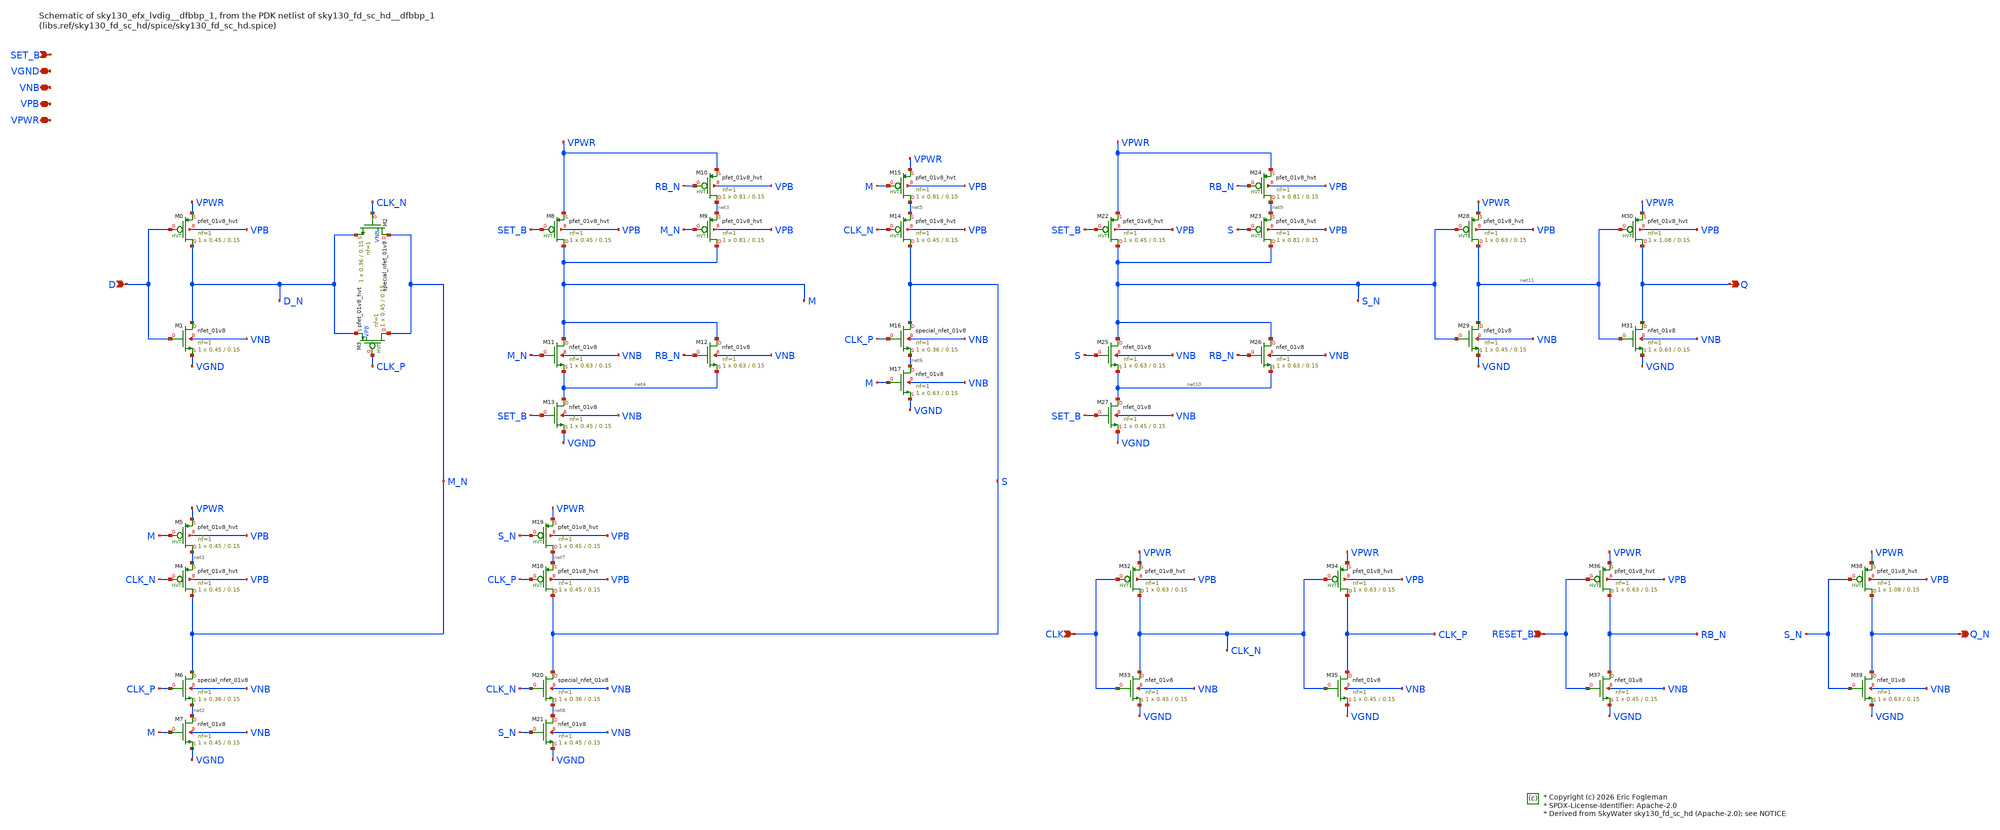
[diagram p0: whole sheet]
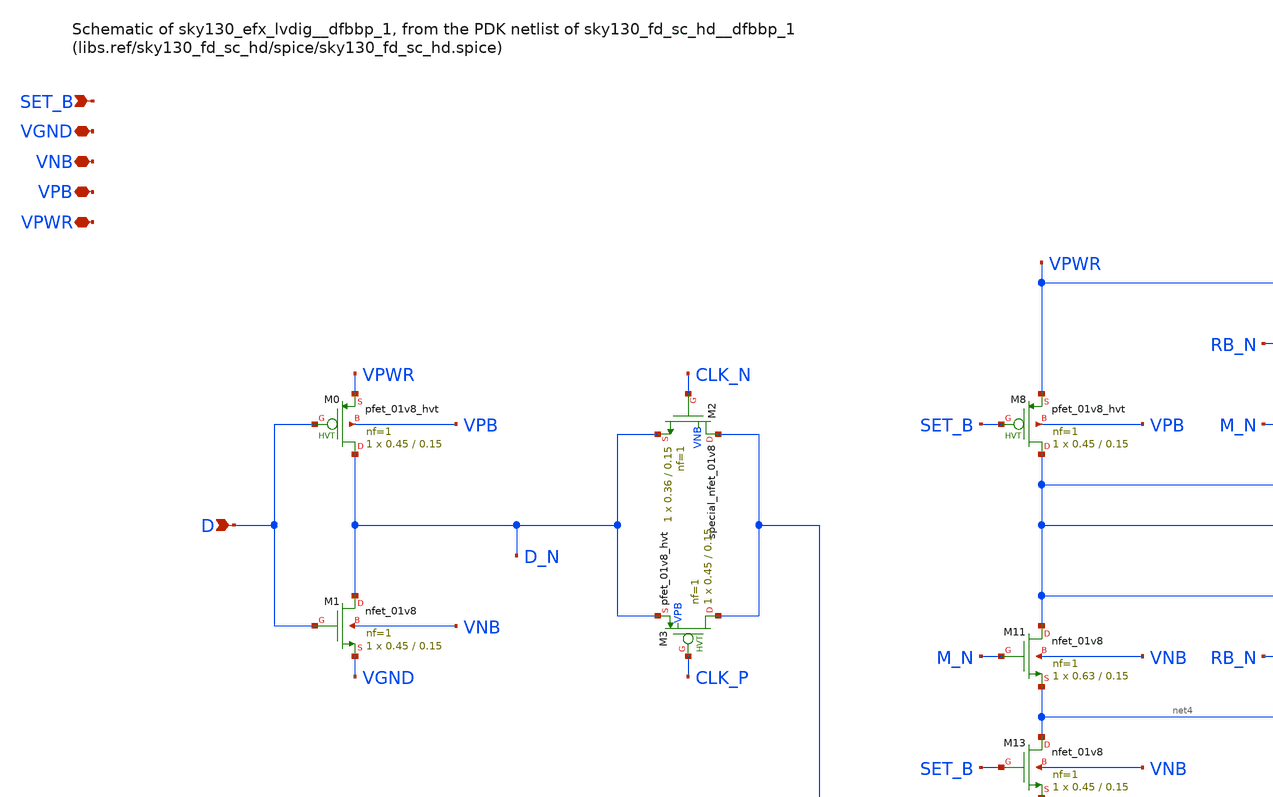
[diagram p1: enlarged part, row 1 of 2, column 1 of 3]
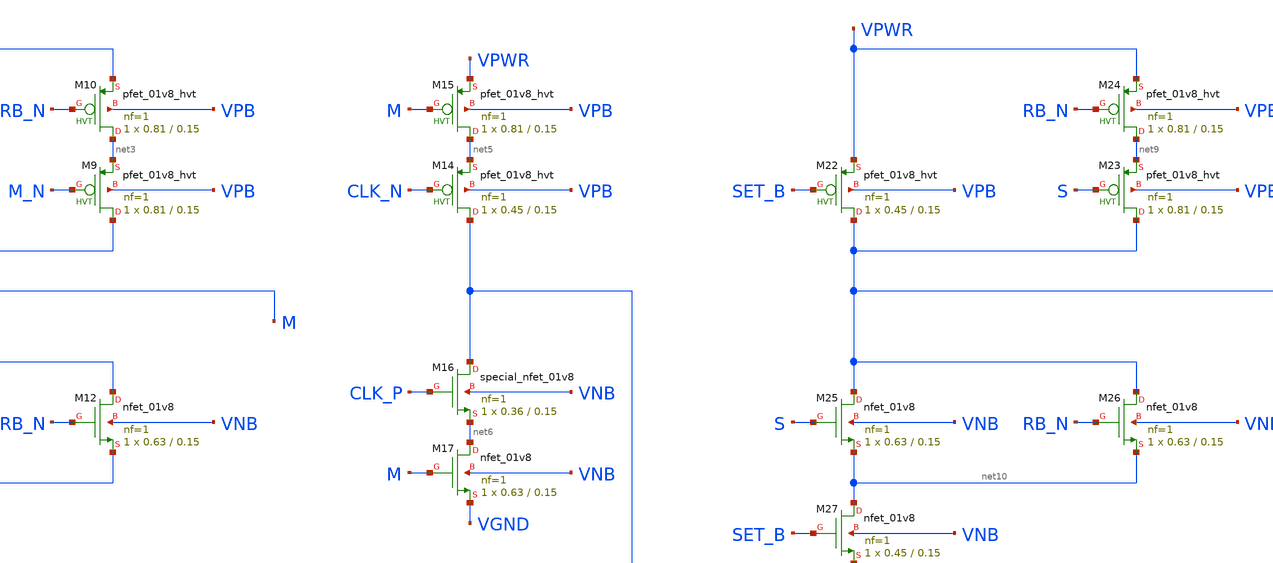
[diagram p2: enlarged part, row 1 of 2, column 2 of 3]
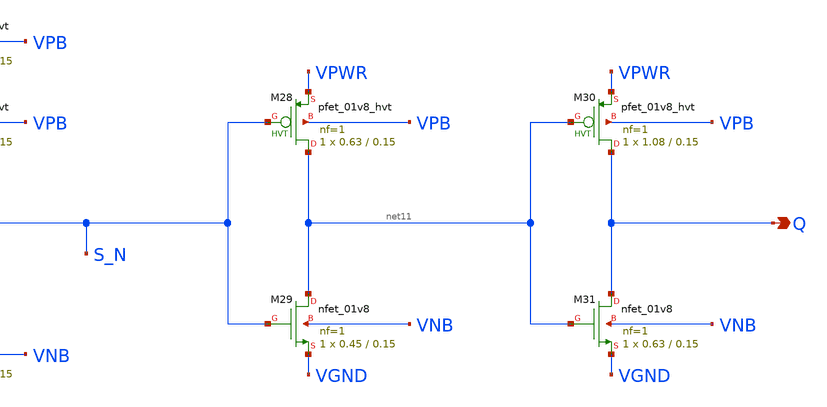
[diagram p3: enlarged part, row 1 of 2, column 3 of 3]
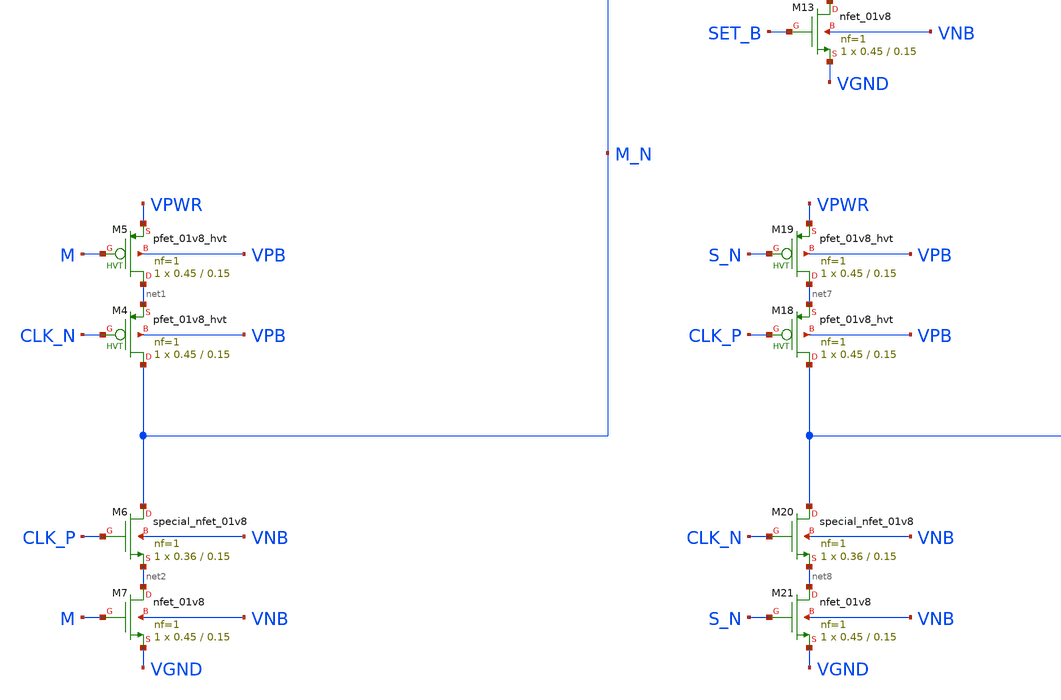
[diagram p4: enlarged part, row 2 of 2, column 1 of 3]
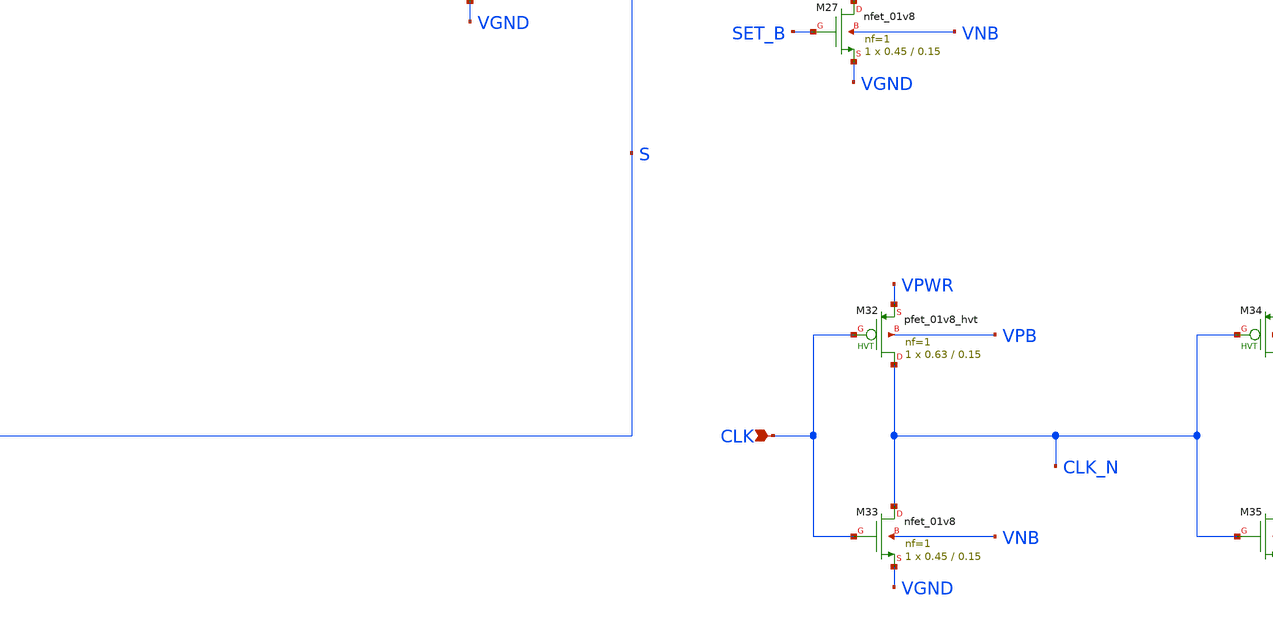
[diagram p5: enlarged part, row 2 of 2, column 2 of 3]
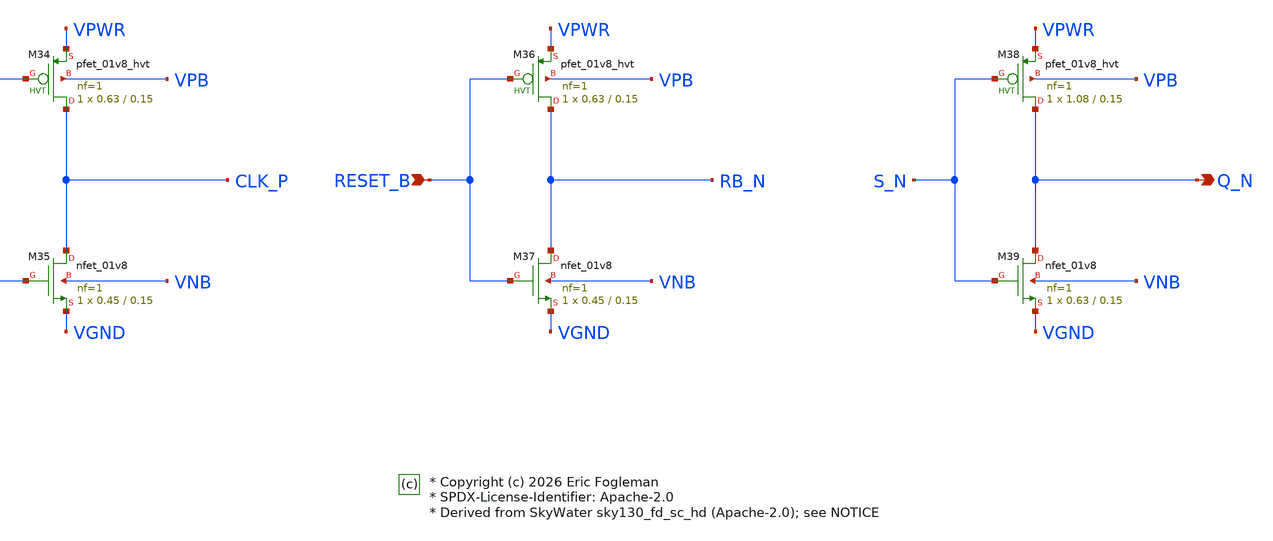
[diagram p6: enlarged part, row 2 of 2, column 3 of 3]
** sch_path: xschem/sky130_efx_lvdig__dfbbp_1.sch

* Copyright (c) 2026 Eric Fogleman
* SPDX-License-Identifier: Apache-2.0
* Derived from SkyWater sky130_fd_sc_hd (Apache-2.0); see NOTICE

**.subckt sky130_efx_lvdig__dfbbp_1 D Q CLK RESET_B Q_N SET_B VGND VNB VPB VPWR
*.ipin D
*.opin Q
*.ipin CLK
*.ipin RESET_B
*.opin Q_N
*.ipin SET_B
*.iopin VGND
*.iopin VNB
*.iopin VPB
*.iopin VPWR
XM0 D_N D VPWR VPB sky130_fd_pr__pfet_01v8_hvt L=0.15 W=0.45 nf=1 ad='int((1 + 1)/2) * 0.45 / 1 * 0.29'
+ as='int((1 + 2)/2) * 0.45 / 1 * 0.29' pd='2*int((1 + 1)/2) * (0.45 / 1 + 0.29)' ps='2*int((1 + 2)/2) * (0.45 / 1 + 0.29)'
+ nrd='0.29 / 0.45 ' nrs='0.29 / 0.45 ' sa=0 sb=0 sd=0 mult=1 m=1
XM1 D_N D VGND VNB sky130_fd_pr__nfet_01v8 L=0.15 W=0.45 nf=1 ad='int((1 + 1)/2) * 0.45 / 1 * 0.29' as='int((1 + 2)/2) * 0.45 / 1 * 0.29'
+ pd='2*int((1 + 1)/2) * (0.45 / 1 + 0.29)' ps='2*int((1 + 2)/2) * (0.45 / 1 + 0.29)' nrd='0.29 / 0.45 '
+ nrs='0.29 / 0.45 ' sa=0 sb=0 sd=0 mult=1 m=1
XM2 M_N CLK_N D_N VNB sky130_fd_pr__special_nfet_01v8 L=0.15 W=0.36 nf=1 ad='int((nf+1)/2) * W/nf * 0.29'
+ as='int((nf+2)/2) * W/nf * 0.29' pd='2*int((nf+1)/2) * (W/nf + 0.29)' ps='2*int((nf+2)/2) * (W/nf + 0.29)'
+ nrd='0.29 / W' nrs='0.29 / W' sa=0 sb=0 sd=0 mult=1 m=1
XM3 M_N CLK_P D_N VPB sky130_fd_pr__pfet_01v8_hvt L=0.15 W=0.45 nf=1 ad='int((1 + 1)/2) * 0.45 / 1 * 0.29'
+ as='int((1 + 2)/2) * 0.45 / 1 * 0.29' pd='2*int((1 + 1)/2) * (0.45 / 1 + 0.29)' ps='2*int((1 + 2)/2) * (0.45 / 1 + 0.29)'
+ nrd='0.29 / 0.45 ' nrs='0.29 / 0.45 ' sa=0 sb=0 sd=0 mult=1 m=1
XM4 M_N CLK_N net1 VPB sky130_fd_pr__pfet_01v8_hvt L=0.15 W=0.45 nf=1 ad='int((1 + 1)/2) * 0.45 / 1 * 0.29'
+ as='int((1 + 2)/2) * 0.45 / 1 * 0.29' pd='2*int((1 + 1)/2) * (0.45 / 1 + 0.29)' ps='2*int((1 + 2)/2) * (0.45 / 1 + 0.29)'
+ nrd='0.29 / 0.45 ' nrs='0.29 / 0.45 ' sa=0 sb=0 sd=0 mult=1 m=1
XM5 net1 M VPWR VPB sky130_fd_pr__pfet_01v8_hvt L=0.15 W=0.45 nf=1 ad='int((1 + 1)/2) * 0.45 / 1 * 0.29'
+ as='int((1 + 2)/2) * 0.45 / 1 * 0.29' pd='2*int((1 + 1)/2) * (0.45 / 1 + 0.29)' ps='2*int((1 + 2)/2) * (0.45 / 1 + 0.29)'
+ nrd='0.29 / 0.45 ' nrs='0.29 / 0.45 ' sa=0 sb=0 sd=0 mult=1 m=1
XM6 M_N CLK_P net2 VNB sky130_fd_pr__special_nfet_01v8 L=0.15 W=0.36 nf=1 ad='int((1 + 1)/2) * 0.36 / 1 * 0.29'
+ as='int((1 + 2)/2) * 0.36 / 1 * 0.29' pd='2*int((1 + 1)/2) * (0.36 / 1 + 0.29)' ps='2*int((1 + 2)/2) * (0.36 / 1 + 0.29)'
+ nrd='0.29 / 0.36 ' nrs='0.29 / 0.36 ' sa=0 sb=0 sd=0 mult=1 m=1
XM7 net2 M VGND VNB sky130_fd_pr__nfet_01v8 L=0.15 W=0.45 nf=1 ad='int((1 + 1)/2) * 0.45 / 1 * 0.29'
+ as='int((1 + 2)/2) * 0.45 / 1 * 0.29' pd='2*int((1 + 1)/2) * (0.45 / 1 + 0.29)' ps='2*int((1 + 2)/2) * (0.45 / 1 + 0.29)'
+ nrd='0.29 / 0.45 ' nrs='0.29 / 0.45 ' sa=0 sb=0 sd=0 mult=1 m=1
XM8 M SET_B VPWR VPB sky130_fd_pr__pfet_01v8_hvt L=0.15 W=0.45 nf=1 ad='int((1 + 1)/2) * 0.45 / 1 * 0.29'
+ as='int((1 + 2)/2) * 0.45 / 1 * 0.29' pd='2*int((1 + 1)/2) * (0.45 / 1 + 0.29)' ps='2*int((1 + 2)/2) * (0.45 / 1 + 0.29)'
+ nrd='0.29 / 0.45 ' nrs='0.29 / 0.45 ' sa=0 sb=0 sd=0 mult=1 m=1
XM9 M M_N net3 VPB sky130_fd_pr__pfet_01v8_hvt L=0.15 W=0.81 nf=1 ad='int((1 + 1)/2) * 0.81 / 1 * 0.29'
+ as='int((1 + 2)/2) * 0.81 / 1 * 0.29' pd='2*int((1 + 1)/2) * (0.81 / 1 + 0.29)' ps='2*int((1 + 2)/2) * (0.81 / 1 + 0.29)'
+ nrd='0.29 / 0.81 ' nrs='0.29 / 0.81 ' sa=0 sb=0 sd=0 mult=1 m=1
XM10 net3 RB_N VPWR VPB sky130_fd_pr__pfet_01v8_hvt L=0.15 W=0.81 nf=1 ad='int((1 + 1)/2) * 0.81 / 1 * 0.29'
+ as='int((1 + 2)/2) * 0.81 / 1 * 0.29' pd='2*int((1 + 1)/2) * (0.81 / 1 + 0.29)' ps='2*int((1 + 2)/2) * (0.81 / 1 + 0.29)'
+ nrd='0.29 / 0.81 ' nrs='0.29 / 0.81 ' sa=0 sb=0 sd=0 mult=1 m=1
XM11 M M_N net4 VNB sky130_fd_pr__nfet_01v8 L=0.15 W=0.63 nf=1 ad='int((1 + 1)/2) * 0.63 / 1 * 0.29'
+ as='int((1 + 2)/2) * 0.63 / 1 * 0.29' pd='2*int((1 + 1)/2) * (0.63 / 1 + 0.29)' ps='2*int((1 + 2)/2) * (0.63 / 1 + 0.29)'
+ nrd='0.29 / 0.63 ' nrs='0.29 / 0.63 ' sa=0 sb=0 sd=0 mult=1 m=1
XM12 M RB_N net4 VNB sky130_fd_pr__nfet_01v8 L=0.15 W=0.63 nf=1 ad='int((1 + 1)/2) * 0.63 / 1 * 0.29'
+ as='int((1 + 2)/2) * 0.63 / 1 * 0.29' pd='2*int((1 + 1)/2) * (0.63 / 1 + 0.29)' ps='2*int((1 + 2)/2) * (0.63 / 1 + 0.29)'
+ nrd='0.29 / 0.63 ' nrs='0.29 / 0.63 ' sa=0 sb=0 sd=0 mult=1 m=1
XM13 net4 SET_B VGND VNB sky130_fd_pr__nfet_01v8 L=0.15 W=0.45 nf=1 ad='int((1 + 1)/2) * 0.45 / 1 * 0.29'
+ as='int((1 + 2)/2) * 0.45 / 1 * 0.29' pd='2*int((1 + 1)/2) * (0.45 / 1 + 0.29)' ps='2*int((1 + 2)/2) * (0.45 / 1 + 0.29)'
+ nrd='0.29 / 0.45 ' nrs='0.29 / 0.45 ' sa=0 sb=0 sd=0 mult=1 m=1
XM14 S CLK_N net5 VPB sky130_fd_pr__pfet_01v8_hvt L=0.15 W=0.45 nf=1 ad='int((1 + 1)/2) * 0.45 / 1 * 0.29'
+ as='int((1 + 2)/2) * 0.45 / 1 * 0.29' pd='2*int((1 + 1)/2) * (0.45 / 1 + 0.29)' ps='2*int((1 + 2)/2) * (0.45 / 1 + 0.29)'
+ nrd='0.29 / 0.45 ' nrs='0.29 / 0.45 ' sa=0 sb=0 sd=0 mult=1 m=1
XM15 net5 M VPWR VPB sky130_fd_pr__pfet_01v8_hvt L=0.15 W=0.81 nf=1 ad='int((1 + 1)/2) * 0.81 / 1 * 0.29'
+ as='int((1 + 2)/2) * 0.81 / 1 * 0.29' pd='2*int((1 + 1)/2) * (0.81 / 1 + 0.29)' ps='2*int((1 + 2)/2) * (0.81 / 1 + 0.29)'
+ nrd='0.29 / 0.81 ' nrs='0.29 / 0.81 ' sa=0 sb=0 sd=0 mult=1 m=1
XM16 S CLK_P net6 VNB sky130_fd_pr__special_nfet_01v8 L=0.15 W=0.36 nf=1 ad='int((1 + 1)/2) * 0.36 / 1 * 0.29'
+ as='int((1 + 2)/2) * 0.36 / 1 * 0.29' pd='2*int((1 + 1)/2) * (0.36 / 1 + 0.29)' ps='2*int((1 + 2)/2) * (0.36 / 1 + 0.29)'
+ nrd='0.29 / 0.36 ' nrs='0.29 / 0.36 ' sa=0 sb=0 sd=0 mult=1 m=1
XM17 net6 M VGND VNB sky130_fd_pr__nfet_01v8 L=0.15 W=0.63 nf=1 ad='int((1 + 1)/2) * 0.63 / 1 * 0.29'
+ as='int((1 + 2)/2) * 0.63 / 1 * 0.29' pd='2*int((1 + 1)/2) * (0.63 / 1 + 0.29)' ps='2*int((1 + 2)/2) * (0.63 / 1 + 0.29)'
+ nrd='0.29 / 0.63 ' nrs='0.29 / 0.63 ' sa=0 sb=0 sd=0 mult=1 m=1
XM18 S CLK_P net7 VPB sky130_fd_pr__pfet_01v8_hvt L=0.15 W=0.45 nf=1 ad='int((1 + 1)/2) * 0.45 / 1 * 0.29'
+ as='int((1 + 2)/2) * 0.45 / 1 * 0.29' pd='2*int((1 + 1)/2) * (0.45 / 1 + 0.29)' ps='2*int((1 + 2)/2) * (0.45 / 1 + 0.29)'
+ nrd='0.29 / 0.45 ' nrs='0.29 / 0.45 ' sa=0 sb=0 sd=0 mult=1 m=1
XM19 net7 S_N VPWR VPB sky130_fd_pr__pfet_01v8_hvt L=0.15 W=0.45 nf=1 ad='int((1 + 1)/2) * 0.45 / 1 * 0.29'
+ as='int((1 + 2)/2) * 0.45 / 1 * 0.29' pd='2*int((1 + 1)/2) * (0.45 / 1 + 0.29)' ps='2*int((1 + 2)/2) * (0.45 / 1 + 0.29)'
+ nrd='0.29 / 0.45 ' nrs='0.29 / 0.45 ' sa=0 sb=0 sd=0 mult=1 m=1
XM20 S CLK_N net8 VNB sky130_fd_pr__special_nfet_01v8 L=0.15 W=0.36 nf=1 ad='int((1 + 1)/2) * 0.36 / 1 * 0.29'
+ as='int((1 + 2)/2) * 0.36 / 1 * 0.29' pd='2*int((1 + 1)/2) * (0.36 / 1 + 0.29)' ps='2*int((1 + 2)/2) * (0.36 / 1 + 0.29)'
+ nrd='0.29 / 0.36 ' nrs='0.29 / 0.36 ' sa=0 sb=0 sd=0 mult=1 m=1
XM21 net8 S_N VGND VNB sky130_fd_pr__nfet_01v8 L=0.15 W=0.45 nf=1 ad='int((1 + 1)/2) * 0.45 / 1 * 0.29'
+ as='int((1 + 2)/2) * 0.45 / 1 * 0.29' pd='2*int((1 + 1)/2) * (0.45 / 1 + 0.29)' ps='2*int((1 + 2)/2) * (0.45 / 1 + 0.29)'
+ nrd='0.29 / 0.45 ' nrs='0.29 / 0.45 ' sa=0 sb=0 sd=0 mult=1 m=1
XM22 S_N SET_B VPWR VPB sky130_fd_pr__pfet_01v8_hvt L=0.15 W=0.45 nf=1 ad='int((1 + 1)/2) * 0.45 / 1 * 0.29'
+ as='int((1 + 2)/2) * 0.45 / 1 * 0.29' pd='2*int((1 + 1)/2) * (0.45 / 1 + 0.29)' ps='2*int((1 + 2)/2) * (0.45 / 1 + 0.29)'
+ nrd='0.29 / 0.45 ' nrs='0.29 / 0.45 ' sa=0 sb=0 sd=0 mult=1 m=1
XM23 S_N S net9 VPB sky130_fd_pr__pfet_01v8_hvt L=0.15 W=0.81 nf=1 ad='int((1 + 1)/2) * 0.81 / 1 * 0.29'
+ as='int((1 + 2)/2) * 0.81 / 1 * 0.29' pd='2*int((1 + 1)/2) * (0.81 / 1 + 0.29)' ps='2*int((1 + 2)/2) * (0.81 / 1 + 0.29)'
+ nrd='0.29 / 0.81 ' nrs='0.29 / 0.81 ' sa=0 sb=0 sd=0 mult=1 m=1
XM24 net9 RB_N VPWR VPB sky130_fd_pr__pfet_01v8_hvt L=0.15 W=0.81 nf=1 ad='int((1 + 1)/2) * 0.81 / 1 * 0.29'
+ as='int((1 + 2)/2) * 0.81 / 1 * 0.29' pd='2*int((1 + 1)/2) * (0.81 / 1 + 0.29)' ps='2*int((1 + 2)/2) * (0.81 / 1 + 0.29)'
+ nrd='0.29 / 0.81 ' nrs='0.29 / 0.81 ' sa=0 sb=0 sd=0 mult=1 m=1
XM25 S_N S net10 VNB sky130_fd_pr__nfet_01v8 L=0.15 W=0.63 nf=1 ad='int((1 + 1)/2) * 0.63 / 1 * 0.29'
+ as='int((1 + 2)/2) * 0.63 / 1 * 0.29' pd='2*int((1 + 1)/2) * (0.63 / 1 + 0.29)' ps='2*int((1 + 2)/2) * (0.63 / 1 + 0.29)'
+ nrd='0.29 / 0.63 ' nrs='0.29 / 0.63 ' sa=0 sb=0 sd=0 mult=1 m=1
XM26 S_N RB_N net10 VNB sky130_fd_pr__nfet_01v8 L=0.15 W=0.63 nf=1 ad='int((1 + 1)/2) * 0.63 / 1 * 0.29'
+ as='int((1 + 2)/2) * 0.63 / 1 * 0.29' pd='2*int((1 + 1)/2) * (0.63 / 1 + 0.29)' ps='2*int((1 + 2)/2) * (0.63 / 1 + 0.29)'
+ nrd='0.29 / 0.63 ' nrs='0.29 / 0.63 ' sa=0 sb=0 sd=0 mult=1 m=1
XM27 net10 SET_B VGND VNB sky130_fd_pr__nfet_01v8 L=0.15 W=0.45 nf=1 ad='int((1 + 1)/2) * 0.45 / 1 * 0.29'
+ as='int((1 + 2)/2) * 0.45 / 1 * 0.29' pd='2*int((1 + 1)/2) * (0.45 / 1 + 0.29)' ps='2*int((1 + 2)/2) * (0.45 / 1 + 0.29)'
+ nrd='0.29 / 0.45 ' nrs='0.29 / 0.45 ' sa=0 sb=0 sd=0 mult=1 m=1
XM28 net11 S_N VPWR VPB sky130_fd_pr__pfet_01v8_hvt L=0.15 W=0.63 nf=1 ad='int((1 + 1)/2) * 0.63 / 1 * 0.29'
+ as='int((1 + 2)/2) * 0.63 / 1 * 0.29' pd='2*int((1 + 1)/2) * (0.63 / 1 + 0.29)' ps='2*int((1 + 2)/2) * (0.63 / 1 + 0.29)'
+ nrd='0.29 / 0.63 ' nrs='0.29 / 0.63 ' sa=0 sb=0 sd=0 mult=1 m=1
XM29 net11 S_N VGND VNB sky130_fd_pr__nfet_01v8 L=0.15 W=0.45 nf=1 ad='int((1 + 1)/2) * 0.45 / 1 * 0.29'
+ as='int((1 + 2)/2) * 0.45 / 1 * 0.29' pd='2*int((1 + 1)/2) * (0.45 / 1 + 0.29)' ps='2*int((1 + 2)/2) * (0.45 / 1 + 0.29)'
+ nrd='0.29 / 0.45 ' nrs='0.29 / 0.45 ' sa=0 sb=0 sd=0 mult=1 m=1
XM30 Q net11 VPWR VPB sky130_fd_pr__pfet_01v8_hvt L=0.15 W=1.08 nf=1 ad='int((1 + 1)/2) * 1.08 / 1 * 0.29'
+ as='int((1 + 2)/2) * 1.08 / 1 * 0.29' pd='2*int((1 + 1)/2) * (1.08 / 1 + 0.29)' ps='2*int((1 + 2)/2) * (1.08 / 1 + 0.29)'
+ nrd='0.29 / 1.08 ' nrs='0.29 / 1.08 ' sa=0 sb=0 sd=0 mult=1 m=1
XM31 Q net11 VGND VNB sky130_fd_pr__nfet_01v8 L=0.15 W=0.63 nf=1 ad='int((1 + 1)/2) * 0.63 / 1 * 0.29'
+ as='int((1 + 2)/2) * 0.63 / 1 * 0.29' pd='2*int((1 + 1)/2) * (0.63 / 1 + 0.29)' ps='2*int((1 + 2)/2) * (0.63 / 1 + 0.29)'
+ nrd='0.29 / 0.63 ' nrs='0.29 / 0.63 ' sa=0 sb=0 sd=0 mult=1 m=1
XM32 CLK_N CLK VPWR VPB sky130_fd_pr__pfet_01v8_hvt L=0.15 W=0.63 nf=1 ad='int((1 + 1)/2) * 0.63 / 1 * 0.29'
+ as='int((1 + 2)/2) * 0.63 / 1 * 0.29' pd='2*int((1 + 1)/2) * (0.63 / 1 + 0.29)' ps='2*int((1 + 2)/2) * (0.63 / 1 + 0.29)'
+ nrd='0.29 / 0.63 ' nrs='0.29 / 0.63 ' sa=0 sb=0 sd=0 mult=1 m=1
XM33 CLK_N CLK VGND VNB sky130_fd_pr__nfet_01v8 L=0.15 W=0.45 nf=1 ad='int((1 + 1)/2) * 0.45 / 1 * 0.29'
+ as='int((1 + 2)/2) * 0.45 / 1 * 0.29' pd='2*int((1 + 1)/2) * (0.45 / 1 + 0.29)' ps='2*int((1 + 2)/2) * (0.45 / 1 + 0.29)'
+ nrd='0.29 / 0.45 ' nrs='0.29 / 0.45 ' sa=0 sb=0 sd=0 mult=1 m=1
XM34 CLK_P CLK_N VPWR VPB sky130_fd_pr__pfet_01v8_hvt L=0.15 W=0.63 nf=1 ad='int((1 + 1)/2) * 0.63 / 1 * 0.29'
+ as='int((1 + 2)/2) * 0.63 / 1 * 0.29' pd='2*int((1 + 1)/2) * (0.63 / 1 + 0.29)' ps='2*int((1 + 2)/2) * (0.63 / 1 + 0.29)'
+ nrd='0.29 / 0.63 ' nrs='0.29 / 0.63 ' sa=0 sb=0 sd=0 mult=1 m=1
XM35 CLK_P CLK_N VGND VNB sky130_fd_pr__nfet_01v8 L=0.15 W=0.45 nf=1 ad='int((1 + 1)/2) * 0.45 / 1 * 0.29'
+ as='int((1 + 2)/2) * 0.45 / 1 * 0.29' pd='2*int((1 + 1)/2) * (0.45 / 1 + 0.29)' ps='2*int((1 + 2)/2) * (0.45 / 1 + 0.29)'
+ nrd='0.29 / 0.45 ' nrs='0.29 / 0.45 ' sa=0 sb=0 sd=0 mult=1 m=1
XM36 RB_N RESET_B VPWR VPB sky130_fd_pr__pfet_01v8_hvt L=0.15 W=0.63 nf=1 ad='int((1 + 1)/2) * 0.63 / 1 * 0.29'
+ as='int((1 + 2)/2) * 0.63 / 1 * 0.29' pd='2*int((1 + 1)/2) * (0.63 / 1 + 0.29)' ps='2*int((1 + 2)/2) * (0.63 / 1 + 0.29)'
+ nrd='0.29 / 0.63 ' nrs='0.29 / 0.63 ' sa=0 sb=0 sd=0 mult=1 m=1
XM37 RB_N RESET_B VGND VNB sky130_fd_pr__nfet_01v8 L=0.15 W=0.45 nf=1 ad='int((1 + 1)/2) * 0.45 / 1 * 0.29'
+ as='int((1 + 2)/2) * 0.45 / 1 * 0.29' pd='2*int((1 + 1)/2) * (0.45 / 1 + 0.29)' ps='2*int((1 + 2)/2) * (0.45 / 1 + 0.29)'
+ nrd='0.29 / 0.45 ' nrs='0.29 / 0.45 ' sa=0 sb=0 sd=0 mult=1 m=1
XM38 Q_N S_N VPWR VPB sky130_fd_pr__pfet_01v8_hvt L=0.15 W=1.08 nf=1 ad='int((1 + 1)/2) * 1.08 / 1 * 0.29'
+ as='int((1 + 2)/2) * 1.08 / 1 * 0.29' pd='2*int((1 + 1)/2) * (1.08 / 1 + 0.29)' ps='2*int((1 + 2)/2) * (1.08 / 1 + 0.29)'
+ nrd='0.29 / 1.08 ' nrs='0.29 / 1.08 ' sa=0 sb=0 sd=0 mult=1 m=1
XM39 Q_N S_N VGND VNB sky130_fd_pr__nfet_01v8 L=0.15 W=0.63 nf=1 ad='int((1 + 1)/2) * 0.63 / 1 * 0.29'
+ as='int((1 + 2)/2) * 0.63 / 1 * 0.29' pd='2*int((1 + 1)/2) * (0.63 / 1 + 0.29)' ps='2*int((1 + 2)/2) * (0.63 / 1 + 0.29)'
+ nrd='0.29 / 0.63 ' nrs='0.29 / 0.63 ' sa=0 sb=0 sd=0 mult=1 m=1
**.ends
.end
